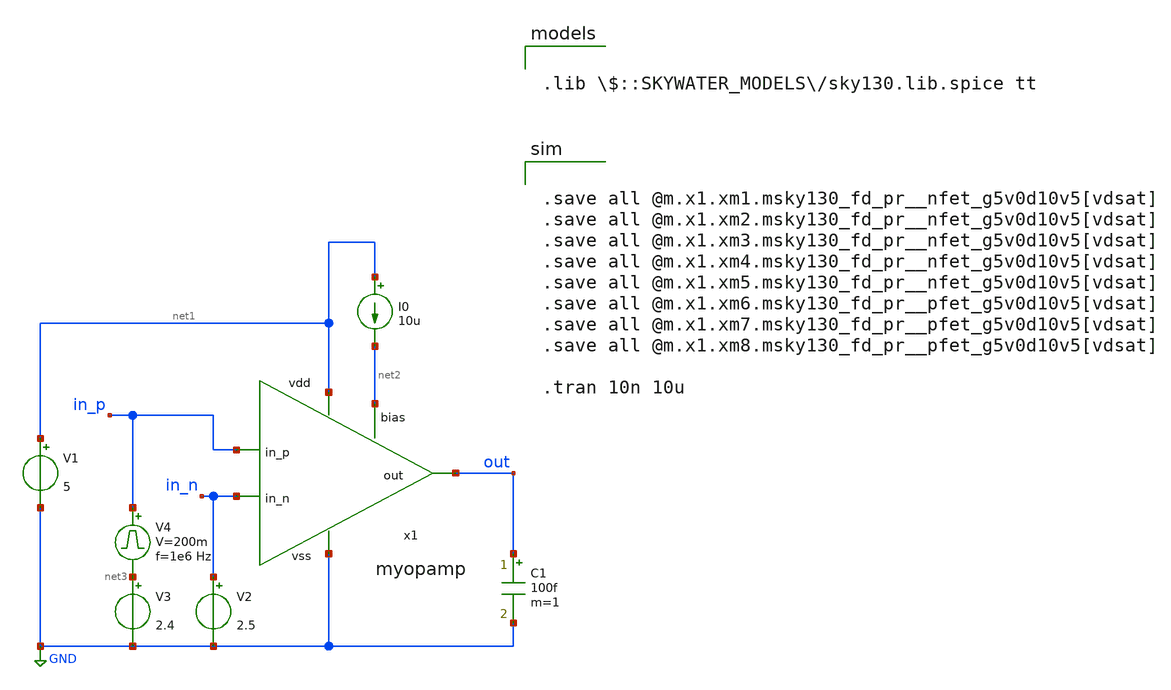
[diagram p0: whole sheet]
** sch_path: design/myopamp/test/tb.sch
**.subckt tb
x1 net1 in_n in_p out net2 GND myopamp
V1 net1 GND 5
I0 net1 net2 10u
V2 in_n GND 2.5
V3 net3 GND 2.4
V4 in_p net3 pulse 0 200m '0.495/ 1e6 ' '0.01/1e6 ' '0.01/1e6 ' '0.49/1e6 ' '1/1e6 '
C1 out GND 100f m=1
**** begin user architecture code


.save all @m.x1.xm1.msky130_fd_pr__nfet_g5v0d10v5[vdsat]
.save all @m.x1.xm2.msky130_fd_pr__nfet_g5v0d10v5[vdsat]
.save all @m.x1.xm3.msky130_fd_pr__nfet_g5v0d10v5[vdsat]
.save all @m.x1.xm4.msky130_fd_pr__nfet_g5v0d10v5[vdsat]
.save all @m.x1.xm5.msky130_fd_pr__nfet_g5v0d10v5[vdsat]
.save all @m.x1.xm6.msky130_fd_pr__pfet_g5v0d10v5[vdsat]
.save all @m.x1.xm7.msky130_fd_pr__pfet_g5v0d10v5[vdsat]
.save all @m.x1.xm8.msky130_fd_pr__pfet_g5v0d10v5[vdsat]

.tran 10n 10u



.lib $::SKYWATER_MODELS/sky130.lib.spice tt

**** end user architecture code
**.ends

* expanding   symbol:  myopamp/myopamp.sym # of pins=6
** sym_path: design/myopamp/myopamp.sym
** sch_path: design/myopamp/myopamp.sch
.subckt myopamp vdd in_n in_p out bias vss
*.ipin in_n
*.ipin in_p
*.ipin bias
*.opin out
*.iopin vdd
*.iopin vss
XM7 vdd net2 net3 vdd sky130_fd_pr__pfet_g5v0d10v5 L=0.5 W=1 nf=1 ad='int((nf+1)/2) * W/nf * 0.29' as='int((nf+2)/2) * W/nf * 0.29'
+ pd='2*int((nf+1)/2) * (W/nf + 0.29)' ps='2*int((nf+2)/2) * (W/nf + 0.29)' nrd='0.29 / W' nrs='0.29 / W'
+ sa=0 sb=0 sd=0 mult=1 m=1
XM6 vdd net2 net2 vdd sky130_fd_pr__pfet_g5v0d10v5 L=0.5 W=1 nf=1 ad='int((nf+1)/2) * W/nf * 0.29' as='int((nf+2)/2) * W/nf * 0.29'
+ pd='2*int((nf+1)/2) * (W/nf + 0.29)' ps='2*int((nf+2)/2) * (W/nf + 0.29)' nrd='0.29 / W' nrs='0.29 / W'
+ sa=0 sb=0 sd=0 mult=1 m=1
XM8 vdd net3 out vdd sky130_fd_pr__pfet_g5v0d10v5 L=0.5 W=1 nf=1 ad='int((nf+1)/2) * W/nf * 0.29' as='int((nf+2)/2) * W/nf * 0.29'
+ pd='2*int((nf+1)/2) * (W/nf + 0.29)' ps='2*int((nf+2)/2) * (W/nf + 0.29)' nrd='0.29 / W' nrs='0.29 / W'
+ sa=0 sb=0 sd=0 mult=1 m=1
XM4 net2 in_n net1 vss sky130_fd_pr__nfet_g5v0d10v5 L=0.5 W=1 nf=1 ad='int((nf+1)/2) * W/nf * 0.29' as='int((nf+2)/2) * W/nf * 0.29'
+ pd='2*int((nf+1)/2) * (W/nf + 0.29)' ps='2*int((nf+2)/2) * (W/nf + 0.29)' nrd='0.29 / W' nrs='0.29 / W'
+ sa=0 sb=0 sd=0 mult=1 m=1
XM5 net3 in_p net1 vss sky130_fd_pr__nfet_g5v0d10v5 L=0.5 W=1 nf=1 ad='int((nf+1)/2) * W/nf * 0.29' as='int((nf+2)/2) * W/nf * 0.29'
+ pd='2*int((nf+1)/2) * (W/nf + 0.29)' ps='2*int((nf+2)/2) * (W/nf + 0.29)' nrd='0.29 / W' nrs='0.29 / W'
+ sa=0 sb=0 sd=0 mult=1 m=1
XM1 bias bias vss vss sky130_fd_pr__nfet_g5v0d10v5 L=0.5 W=1 nf=1 ad='int((nf+1)/2) * W/nf * 0.29' as='int((nf+2)/2) * W/nf * 0.29'
+ pd='2*int((nf+1)/2) * (W/nf + 0.29)' ps='2*int((nf+2)/2) * (W/nf + 0.29)' nrd='0.29 / W' nrs='0.29 / W'
+ sa=0 sb=0 sd=0 mult=1 m=1
XM2 net1 bias vss vss sky130_fd_pr__nfet_g5v0d10v5 L=0.5 W=1 nf=1 ad='int((nf+1)/2) * W/nf * 0.29' as='int((nf+2)/2) * W/nf * 0.29'
+ pd='2*int((nf+1)/2) * (W/nf + 0.29)' ps='2*int((nf+2)/2) * (W/nf + 0.29)' nrd='0.29 / W' nrs='0.29 / W'
+ sa=0 sb=0 sd=0 mult=1 m=1
XM3 out bias vss vss sky130_fd_pr__nfet_g5v0d10v5 L=0.5 W=1 nf=1 ad='int((nf+1)/2) * W/nf * 0.29' as='int((nf+2)/2) * W/nf * 0.29'
+ pd='2*int((nf+1)/2) * (W/nf + 0.29)' ps='2*int((nf+2)/2) * (W/nf + 0.29)' nrd='0.29 / W' nrs='0.29 / W'
+ sa=0 sb=0 sd=0 mult=1 m=1
.ends

.GLOBAL GND
.end
